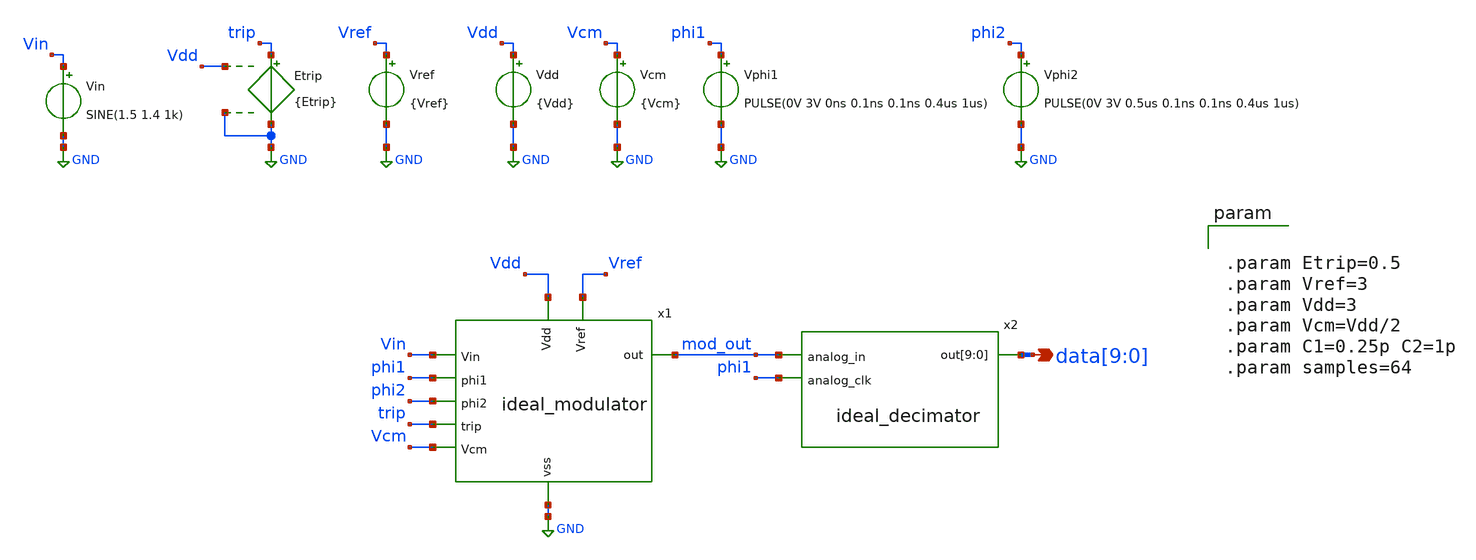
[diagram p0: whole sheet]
** sch_path: 2_ideal_circuits/first_order_delta_sigma_adc.sch
**.subckt first_order_delta_sigma_adc
*+ data[9],data[8],data[7],data[6],data[5],data[4],data[3],data[2],data[1],data[0]
*.opin data[9],data[8],data[7],data[6],data[5],data[4],data[3],data[2],data[1],data[0]
Vin Vin GND SINE(1.5 1.4 1k)
Vref Vref GND {Vref}
Vdd Vdd GND {Vdd}
Vcm Vcm GND {Vcm}
Vphi1 phi1 GND PULSE(0V 3V 0ns 0.1ns 0.1ns 0.4us 1us)
Vphi2 phi2 GND PULSE(0V 3V 0.5us 0.1ns 0.1ns 0.4us 1us)
Etrip trip GND Vdd GND {Etrip}
x1 Vdd Vin mod_out phi1 phi2 trip Vref Vcm GND ideal_modulator
x2 mod_out phi1 data[9] data[8] data[7] data[6] data[5] data[4] data[3] data[2] data[1] data[0] ideal_decimator
+ samples={samples}
**** begin user architecture code


.param Etrip=0.5
.param Vref=3
.param Vdd=3
.param Vcm=Vdd/2
.param C1=0.25p C2=1p
.param samples=64




.temp 27
.control
option sparse
tran 0.1n 5ms 0 20n uic
save V(Vin) V(x1.Vint) V(mod_out) V(Vcm) v(data[9]) v(data[8]) v(data[7]) v(data[6]) v(data[5])
+ v(data[4]) v(data[3]) v(data[2]) v(data[1]) v(data[0])
plot V(Vin) V(x1.Vint) V(mod_out) V(Vcm)

*FFT Analysis
linearize V(mod_out)
fft V(mod_out)
plot db(mag(V(mod_out))) xlimit 10 100k ylimit -80 10

*ADC Output
let digital_val = (v(data[9])*512 + v(data[8])*256 + v(data[7])*128 + v(data[6])*64 + v(data[5])*32
+ + v(data[4])*16 + v(data[3])*8 + v(data[2])*4 + v(data[1])*2 + v(data[0]))/1024
let analog_recon = digital_val * 3.0
plot V(Vin) analog_recon
.endc


**** end user architecture code
**.ends

* expanding   symbol:  ideal_modulator.sym # of pins=9
** sym_path: 2_ideal_circuits/ideal_modulator.sym
** sch_path: 2_ideal_circuits/ideal_modulator.sch
.subckt ideal_modulator Vdd Vin out phi1 phi2 trip Vref Vcm vss
*.opin out
*.ipin Vin
*.ipin phi1
*.ipin trip
*.ipin phi2
*.ipin Vcm
*.ipin Vref
*.ipin Vdd
*.iopin vss
S1 Vin net1 phi1 trip SW1
S2 net1 Vfb phi2 trip SW1
S3 diff net2 phi2 trip SW1
S4 net2 Vcm phi1 trip SW1
x1 Vcm diff Vint ideal_opamp
C2 diff Vint {C2} m=1
C1 net1 net2 {C1} m=1
x3 Vdd cmp Vint Vcm phi1 ideal_comparator
x5 Vfb cmp vss Vref ideal_inverter
x2 out cmp vss Vdd ideal_inverter
.ends


* expanding   symbol:  ideal_decimator.sym # of pins=3
** sym_path: 2_ideal_circuits/ideal_decimator.sym
.include /foss/designs/drms-elie3/2_ideal_circuits/ideal_decimator.cir

* expanding   symbol:  ideal_opamp.sym # of pins=3
** sym_path: ideal_opamp.sym
** sch_path: ideal_opamp.sch
.subckt ideal_opamp inp inn out
*.opin out
*.ipin inp
*.ipin inn
E1 out GND inp inn 1Meg
R1 out GND 100Meg m=1
.ends


* expanding   symbol:  ideal_comparator.sym # of pins=5
** sym_path: 2_ideal_circuits/ideal_comparator.sym
** sch_path: 2_ideal_circuits/ideal_comparator.sch
.subckt ideal_comparator Vdd Vout Vinn Vinp clk
*.ipin Vinp
*.ipin Vinn
*.opin Vout
*.iopin Vdd
*.iopin clk
E1 diff GND Vinp Vinn 1
S1 diff sample tp clk SW1
E2 net1 GND sample GND 1
C1 sample GND 100p m=1
S2 net1 hold clk tp SW1
C2 hold GND 100p m=1
B1 Vout GND V={v(hold)>0?v(Vdd):0}
Etp tp GND Vdd GND 0.5
**** begin user architecture code


.ic v(hold)=1 v(sample)=1


**** end user architecture code
.ends


* expanding   symbol:  ideal_inverter.sym # of pins=4
** sym_path: 2_ideal_circuits/ideal_inverter.sym
** sch_path: 2_ideal_circuits/ideal_inverter.sch
.subckt ideal_inverter out in vss vdd
*.iopin vdd
*.ipin in
*.opin out
*.iopin vss
B1 out GND V={v(in)>v(vdd)/2?v(vss):v(vdd)}
* noconn vdd
* noconn in
* noconn vss
.ends

.GLOBAL GND
**** begin user architecture code
.MODEL SW1 SW( VT=0.9 VH=0.01 RON=0.01 ROFF=10G )
**** end user architecture code
.end
